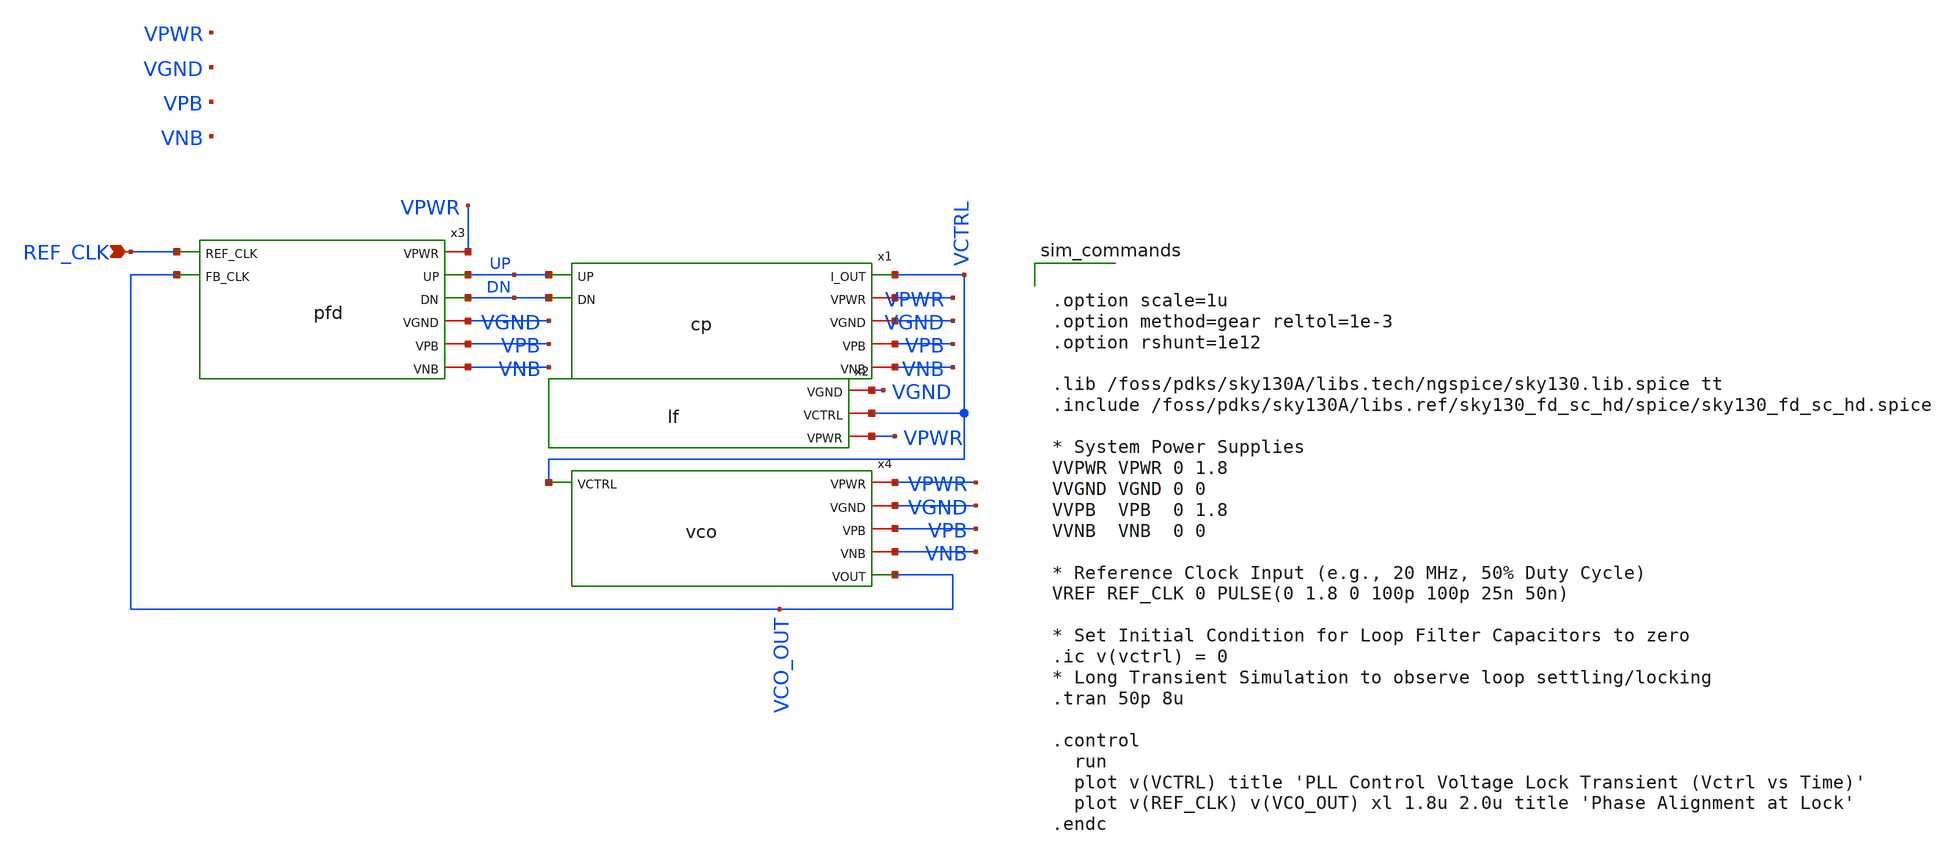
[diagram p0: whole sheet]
** sch_path: pll_top.sch
**.subckt pll_top REF_CLK
*.ipin REF_CLK
x1 UP VCTRL DN VPWR VGND VPB VNB cp
x4 VPWR VGND VPB VNB VCTRL VCO_OUT vco
x3 VPWR UP REF_CLK VCO_OUT DN VGND VPB VNB pfd
x2 VGND VCTRL VPWR lf
**** begin user architecture code


.option scale=1u
.option method=gear reltol=1e-3
.option rshunt=1e12

.lib /foss/pdks/sky130A/libs.tech/ngspice/sky130.lib.spice tt
.include /foss/pdks/sky130A/libs.ref/sky130_fd_sc_hd/spice/sky130_fd_sc_hd.spice

* System Power Supplies
VVPWR VPWR 0 1.8
VVGND VGND 0 0
VVPB  VPB  0 1.8
VVNB  VNB  0 0

* Reference Clock Input (e.g., 20 MHz, 50% Duty Cycle)
VREF REF_CLK 0 PULSE(0 1.8 0 100p 100p 25n 50n)

* Set Initial Condition for Loop Filter Capacitors to zero
.ic v(vctrl) = 0
* Long Transient Simulation to observe loop settling/locking
.tran 50p 8u

.control
  run
  plot v(VCTRL) title 'PLL Control Voltage Lock Transient (Vctrl vs Time)'
  plot v(REF_CLK) v(VCO_OUT) xl 1.8u 2.0u title 'Phase Alignment at Lock'
.endc


**** end user architecture code
**.ends

* expanding   symbol:  cp.sym # of pins=7
** sym_path: cp.sym
** sch_path: cp.sch
.subckt cp UP I_OUT DN VPWR VGND VPB VNB
*.ipin UP
*.ipin DN
*.iopin VPWR
*.iopin VGND
*.iopin VPB
*.iopin VNB
*.opin I_OUT
XMN1 I_OUT net4 net7 VNB sky130_fd_pr__nfet_01v8 L=2 W=4 nf=1 ad='int((1 + 1)/2) * 4 / 1 * 0.29' as='int((1 + 2)/2) * 4 / 1 * 0.29'
+ pd='2*int((1 + 1)/2) * (4 / 1 + 0.29)' ps='2*int((1 + 2)/2) * (4 / 1 + 0.29)' nrd='0.29 / 4 ' nrs='0.29 / 4 '
+ sa=0 sb=0 sd=0 mult=1 m=1
XMP1 I_OUT net3 net6 VPB sky130_fd_pr__pfet_01v8 L=2 W=14 nf=1 ad='int((1 + 1)/2) * 14 / 1 * 0.29' as='int((1 + 2)/2) * 14 / 1 * 0.29'
+ pd='2*int((1 + 1)/2) * (14 / 1 + 0.29)' ps='2*int((1 + 2)/2) * (14 / 1 + 0.29)' nrd='0.29 / 14 ' nrs='0.29 / 14 '
+ sa=0 sb=0 sd=0 mult=1 m=1
Iref net3 net4 20u
XMN2 net7 net2 VGND VNB sky130_fd_pr__nfet_01v8 L=0.5 W=1 nf=1 ad='int((1 + 1)/2) * 1 / 1 * 0.29' as='int((1 + 2)/2) * 1 / 1 * 0.29'
+ pd='2*int((1 + 1)/2) * (1 / 1 + 0.29)' ps='2*int((1 + 2)/2) * (1 / 1 + 0.29)' nrd='0.29 / 1 ' nrs='0.29 / 1 '
+ sa=0 sb=0 sd=0 mult=1 m=1
XMP2 net6 net1 VPWR VPB sky130_fd_pr__pfet_01v8 L=0.5 W=3 nf=1 ad='int((1 + 1)/2) * 3 / 1 * 0.29' as='int((1 + 2)/2) * 3 / 1 * 0.29'
+ pd='2*int((1 + 1)/2) * (3 / 1 + 0.29)' ps='2*int((1 + 2)/2) * (3 / 1 + 0.29)' nrd='0.29 / 3 ' nrs='0.29 / 3 '
+ sa=0 sb=0 sd=0 mult=1 m=1
x1 UP VGND VNB VPB VPWR net1 sky130_fd_sc_hd__inv_1
XMP3 net3 net3 VPWR VPB sky130_fd_pr__pfet_01v8 L=2 W=14 nf=1 ad='int((1 + 1)/2) * 14 / 1 * 0.29' as='int((1 + 2)/2) * 14 / 1 * 0.29'
+ pd='2*int((1 + 1)/2) * (14 / 1 + 0.29)' ps='2*int((1 + 2)/2) * (14 / 1 + 0.29)' nrd='0.29 / 14 ' nrs='0.29 / 14 '
+ sa=0 sb=0 sd=0 mult=1 m=1
XMN3 net4 net4 VGND VNB sky130_fd_pr__nfet_01v8 L=2 W=4 nf=1 ad='int((1 + 1)/2) * 4 / 1 * 0.29' as='int((1 + 2)/2) * 4 / 1 * 0.29'
+ pd='2*int((1 + 1)/2) * (4 / 1 + 0.29)' ps='2*int((1 + 2)/2) * (4 / 1 + 0.29)' nrd='0.29 / 4 ' nrs='0.29 / 4 '
+ sa=0 sb=0 sd=0 mult=1 m=1
x2 DN VGND VNB VPB VPWR net5 sky130_fd_sc_hd__inv_1
x3 net5 VGND VNB VPB VPWR net2 sky130_fd_sc_hd__inv_1
.ends


* expanding   symbol:  vco.sym # of pins=6
** sym_path: vco.sym
** sch_path: vco.sch
.subckt vco VPWR VGND VPB VNB VCTRL VOUT
*.iopin VPWR
*.iopin VGND
*.iopin VPB
*.iopin VNB
*.opin VOUT
*.ipin VCTRL
XM1 vpctrl VCTRL VGND VNB sky130_fd_pr__nfet_01v8 L=0.5 W=1 nf=1 ad='int((1 + 1)/2) * 1 / 1 * 0.29' as='int((1 + 2)/2) * 1 / 1 * 0.29'
+ pd='2*int((1 + 1)/2) * (1 / 1 + 0.29)' ps='2*int((1 + 2)/2) * (1 / 1 + 0.29)' nrd='0.29 / 1 ' nrs='0.29 / 1 '
+ sa=0 sb=0 sd=0 mult=1 m=1
XM2 vpctrl vpctrl VPWR VPB sky130_fd_pr__pfet_01v8 L=0.5 W=3 nf=1 ad='int((1 + 1)/2) * 3 / 1 * 0.29'
+ as='int((1 + 2)/2) * 3 / 1 * 0.29' pd='2*int((1 + 1)/2) * (3 / 1 + 0.29)' ps='2*int((1 + 2)/2) * (3 / 1 + 0.29)'
+ nrd='0.29 / 3 ' nrs='0.29 / 3 ' sa=0 sb=0 sd=0 mult=1 m=1
XM11 net1 R_OUT net6 VNB sky130_fd_pr__nfet_01v8 L=0.15 W=1 nf=1 ad='int((1 + 1)/2) * 1 / 1 * 0.29' as='int((1 + 2)/2) * 1 / 1 * 0.29'
+ pd='2*int((1 + 1)/2) * (1 / 1 + 0.29)' ps='2*int((1 + 2)/2) * (1 / 1 + 0.29)' nrd='0.29 / 1 ' nrs='0.29 / 1 '
+ sa=0 sb=0 sd=0 mult=1 m=1
XM12 net1 R_OUT net5 VPB sky130_fd_pr__pfet_01v8 L=0.15 W=1 nf=1 ad='int((1 + 1)/2) * 1 / 1 * 0.29' as='int((1 + 2)/2) * 1 / 1 * 0.29'
+ pd='2*int((1 + 1)/2) * (1 / 1 + 0.29)' ps='2*int((1 + 2)/2) * (1 / 1 + 0.29)' nrd='0.29 / 1 ' nrs='0.29 / 1 '
+ sa=0 sb=0 sd=0 mult=1 m=1
XM13 net5 vpctrl VPWR VPB sky130_fd_pr__pfet_01v8 L=0.5 W=3 nf=1 ad='int((1 + 1)/2) * 3 / 1 * 0.29' as='int((1 + 2)/2) * 3 / 1 * 0.29'
+ pd='2*int((1 + 1)/2) * (3 / 1 + 0.29)' ps='2*int((1 + 2)/2) * (3 / 1 + 0.29)' nrd='0.29 / 3 ' nrs='0.29 / 3 '
+ sa=0 sb=0 sd=0 mult=1 m=1
XM14 net6 VCTRL VGND VNB sky130_fd_pr__nfet_01v8 L=0.5 W=1 nf=1 ad='int((1 + 1)/2) * 1 / 1 * 0.29' as='int((1 + 2)/2) * 1 / 1 * 0.29'
+ pd='2*int((1 + 1)/2) * (1 / 1 + 0.29)' ps='2*int((1 + 2)/2) * (1 / 1 + 0.29)' nrd='0.29 / 1 ' nrs='0.29 / 1 '
+ sa=0 sb=0 sd=0 mult=1 m=1
XM3 net2 net1 net8 VNB sky130_fd_pr__nfet_01v8 L=0.15 W=1 nf=1 ad='int((1 + 1)/2) * 1 / 1 * 0.29' as='int((1 + 2)/2) * 1 / 1 * 0.29'
+ pd='2*int((1 + 1)/2) * (1 / 1 + 0.29)' ps='2*int((1 + 2)/2) * (1 / 1 + 0.29)' nrd='0.29 / 1 ' nrs='0.29 / 1 '
+ sa=0 sb=0 sd=0 mult=1 m=1
XM4 net2 net1 net7 VPB sky130_fd_pr__pfet_01v8 L=0.15 W=1 nf=1 ad='int((1 + 1)/2) * 1 / 1 * 0.29' as='int((1 + 2)/2) * 1 / 1 * 0.29'
+ pd='2*int((1 + 1)/2) * (1 / 1 + 0.29)' ps='2*int((1 + 2)/2) * (1 / 1 + 0.29)' nrd='0.29 / 1 ' nrs='0.29 / 1 '
+ sa=0 sb=0 sd=0 mult=1 m=1
XM15 net7 vpctrl VPWR VPB sky130_fd_pr__pfet_01v8 L=0.5 W=3 nf=1 ad='int((1 + 1)/2) * 3 / 1 * 0.29' as='int((1 + 2)/2) * 3 / 1 * 0.29'
+ pd='2*int((1 + 1)/2) * (3 / 1 + 0.29)' ps='2*int((1 + 2)/2) * (3 / 1 + 0.29)' nrd='0.29 / 3 ' nrs='0.29 / 3 '
+ sa=0 sb=0 sd=0 mult=1 m=1
XM16 net8 VCTRL VGND VNB sky130_fd_pr__nfet_01v8 L=0.5 W=1 nf=1 ad='int((1 + 1)/2) * 1 / 1 * 0.29' as='int((1 + 2)/2) * 1 / 1 * 0.29'
+ pd='2*int((1 + 1)/2) * (1 / 1 + 0.29)' ps='2*int((1 + 2)/2) * (1 / 1 + 0.29)' nrd='0.29 / 1 ' nrs='0.29 / 1 '
+ sa=0 sb=0 sd=0 mult=1 m=1
XM5 net3 net2 net10 VNB sky130_fd_pr__nfet_01v8 L=0.15 W=1 nf=1 ad='int((1 + 1)/2) * 1 / 1 * 0.29' as='int((1 + 2)/2) * 1 / 1 * 0.29'
+ pd='2*int((1 + 1)/2) * (1 / 1 + 0.29)' ps='2*int((1 + 2)/2) * (1 / 1 + 0.29)' nrd='0.29 / 1 ' nrs='0.29 / 1 '
+ sa=0 sb=0 sd=0 mult=1 m=1
XM6 net3 net2 net9 VPB sky130_fd_pr__pfet_01v8 L=0.15 W=1 nf=1 ad='int((1 + 1)/2) * 1 / 1 * 0.29' as='int((1 + 2)/2) * 1 / 1 * 0.29'
+ pd='2*int((1 + 1)/2) * (1 / 1 + 0.29)' ps='2*int((1 + 2)/2) * (1 / 1 + 0.29)' nrd='0.29 / 1 ' nrs='0.29 / 1 '
+ sa=0 sb=0 sd=0 mult=1 m=1
XM7 net9 vpctrl VPWR VPB sky130_fd_pr__pfet_01v8 L=0.5 W=3 nf=1 ad='int((1 + 1)/2) * 3 / 1 * 0.29' as='int((1 + 2)/2) * 3 / 1 * 0.29'
+ pd='2*int((1 + 1)/2) * (3 / 1 + 0.29)' ps='2*int((1 + 2)/2) * (3 / 1 + 0.29)' nrd='0.29 / 3 ' nrs='0.29 / 3 '
+ sa=0 sb=0 sd=0 mult=1 m=1
XM8 net10 VCTRL VGND VNB sky130_fd_pr__nfet_01v8 L=0.5 W=1 nf=1 ad='int((1 + 1)/2) * 1 / 1 * 0.29' as='int((1 + 2)/2) * 1 / 1 * 0.29'
+ pd='2*int((1 + 1)/2) * (1 / 1 + 0.29)' ps='2*int((1 + 2)/2) * (1 / 1 + 0.29)' nrd='0.29 / 1 ' nrs='0.29 / 1 '
+ sa=0 sb=0 sd=0 mult=1 m=1
XM9 net4 net3 net12 VNB sky130_fd_pr__nfet_01v8 L=0.15 W=1 nf=1 ad='int((1 + 1)/2) * 1 / 1 * 0.29' as='int((1 + 2)/2) * 1 / 1 * 0.29'
+ pd='2*int((1 + 1)/2) * (1 / 1 + 0.29)' ps='2*int((1 + 2)/2) * (1 / 1 + 0.29)' nrd='0.29 / 1 ' nrs='0.29 / 1 '
+ sa=0 sb=0 sd=0 mult=1 m=1
XM10 net4 net3 net11 VPB sky130_fd_pr__pfet_01v8 L=0.15 W=1 nf=1 ad='int((1 + 1)/2) * 1 / 1 * 0.29' as='int((1 + 2)/2) * 1 / 1 * 0.29'
+ pd='2*int((1 + 1)/2) * (1 / 1 + 0.29)' ps='2*int((1 + 2)/2) * (1 / 1 + 0.29)' nrd='0.29 / 1 ' nrs='0.29 / 1 '
+ sa=0 sb=0 sd=0 mult=1 m=1
XM17 net11 vpctrl VPWR VPB sky130_fd_pr__pfet_01v8 L=0.5 W=3 nf=1 ad='int((1 + 1)/2) * 3 / 1 * 0.29'
+ as='int((1 + 2)/2) * 3 / 1 * 0.29' pd='2*int((1 + 1)/2) * (3 / 1 + 0.29)' ps='2*int((1 + 2)/2) * (3 / 1 + 0.29)'
+ nrd='0.29 / 3 ' nrs='0.29 / 3 ' sa=0 sb=0 sd=0 mult=1 m=1
XM18 net12 VCTRL VGND VNB sky130_fd_pr__nfet_01v8 L=0.5 W=1 nf=1 ad='int((1 + 1)/2) * 1 / 1 * 0.29' as='int((1 + 2)/2) * 1 / 1 * 0.29'
+ pd='2*int((1 + 1)/2) * (1 / 1 + 0.29)' ps='2*int((1 + 2)/2) * (1 / 1 + 0.29)' nrd='0.29 / 1 ' nrs='0.29 / 1 '
+ sa=0 sb=0 sd=0 mult=1 m=1
XM19 R_OUT net4 net14 VNB sky130_fd_pr__nfet_01v8 L=0.15 W=1 nf=1 ad='int((1 + 1)/2) * 1 / 1 * 0.29'
+ as='int((1 + 2)/2) * 1 / 1 * 0.29' pd='2*int((1 + 1)/2) * (1 / 1 + 0.29)' ps='2*int((1 + 2)/2) * (1 / 1 + 0.29)'
+ nrd='0.29 / 1 ' nrs='0.29 / 1 ' sa=0 sb=0 sd=0 mult=1 m=1
XM20 R_OUT net4 net13 VPB sky130_fd_pr__pfet_01v8 L=0.15 W=1 nf=1 ad='int((1 + 1)/2) * 1 / 1 * 0.29'
+ as='int((1 + 2)/2) * 1 / 1 * 0.29' pd='2*int((1 + 1)/2) * (1 / 1 + 0.29)' ps='2*int((1 + 2)/2) * (1 / 1 + 0.29)'
+ nrd='0.29 / 1 ' nrs='0.29 / 1 ' sa=0 sb=0 sd=0 mult=1 m=1
XM21 net13 vpctrl VPWR VPB sky130_fd_pr__pfet_01v8 L=0.5 W=3 nf=1 ad='int((1 + 1)/2) * 3 / 1 * 0.29'
+ as='int((1 + 2)/2) * 3 / 1 * 0.29' pd='2*int((1 + 1)/2) * (3 / 1 + 0.29)' ps='2*int((1 + 2)/2) * (3 / 1 + 0.29)'
+ nrd='0.29 / 3 ' nrs='0.29 / 3 ' sa=0 sb=0 sd=0 mult=1 m=1
XM22 net14 VCTRL VGND VNB sky130_fd_pr__nfet_01v8 L=0.5 W=1 nf=1 ad='int((1 + 1)/2) * 1 / 1 * 0.29' as='int((1 + 2)/2) * 1 / 1 * 0.29'
+ pd='2*int((1 + 1)/2) * (1 / 1 + 0.29)' ps='2*int((1 + 2)/2) * (1 / 1 + 0.29)' nrd='0.29 / 1 ' nrs='0.29 / 1 '
+ sa=0 sb=0 sd=0 mult=1 m=1
x1 R_OUT VGND VNB VPB VPWR VOUT sky130_fd_sc_hd__inv_1
**** begin user architecture code
OUT
**** end user architecture code
.ends


* expanding   symbol:  pfd.sym # of pins=8
** sym_path: pfd.sym
** sch_path: pfd.sch
.subckt pfd VPWR UP REF_CLK FB_CLK DN VGND VPB VNB
*.ipin REF_CLK
*.ipin FB_CLK
*.iopin VGND
*.iopin VPB
*.iopin VNB
*.iopin VPWR
*.opin UP
*.opin DN
x1 REF_CLK VPWR RST_B VGND VNB VPB VPWR UP sky130_fd_sc_hd__dfrtp_1
x2 FB_CLK VPWR RST_B VGND VNB VPB VPWR DN sky130_fd_sc_hd__dfrtp_1
x3 UP DN VGND VNB VPB VPWR RST_RAW sky130_fd_sc_hd__nand2_1
x4 RST_RAW VGND VNB VPB VPWR net1 sky130_fd_sc_hd__inv_1
x5 net1 VGND VNB VPB VPWR RST_B sky130_fd_sc_hd__inv_1
.ends


* expanding   symbol:  lf.sym # of pins=3
** sym_path: lf.sym
** sch_path: lf.sch
.subckt lf VGND VCTRL VPWR
*.iopin VGND
*.iopin VCTRL
*.iopin VPWR
XC1 net1 VGND sky130_fd_pr__cap_mim_m3_1 W=225 L=225 MF=1 m=1
XC2 VCTRL VGND sky130_fd_pr__cap_mim_m3_1 W=71 L=71 MF=1 m=1
XR1 net1 VCTRL VPWR sky130_fd_pr__res_high_po W=1 L=61.9 mult=1 m=1
.ends

.end
